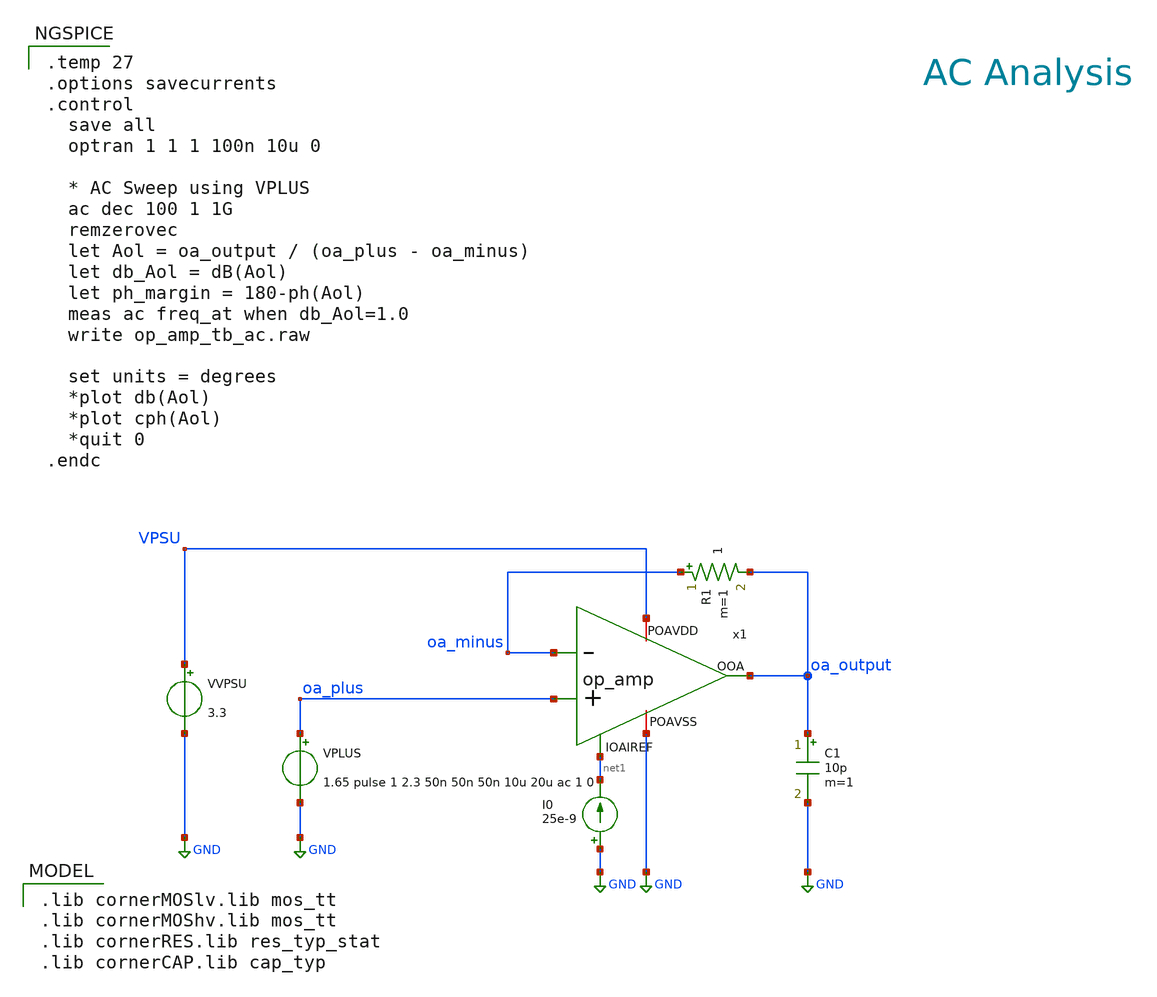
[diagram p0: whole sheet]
** sch_path: xschem/op_amp_tb_ac.sch
**.subckt op_amp_tb_ac
VVPSU VPSU GND 3.3
I0 GND net1 25e-9
x1 VPSU net1 oa_minus oa_output oa_plus GND op_amp
VPLUS oa_plus GND 1.65 pulse 1 2.3 50n 50n 50n 10u 20u ac 1 0
R1 oa_minus oa_output 1 m=1
C1 oa_output GND 10p m=1
**** begin user architecture code

.lib cornerMOSlv.lib mos_tt
.lib cornerMOShv.lib mos_tt
.lib cornerRES.lib res_typ_stat
.lib cornerCAP.lib cap_typ



.temp 27
.options savecurrents
.control
  save all
  optran 1 1 1 100n 10u 0

  * AC Sweep using VPLUS
  ac dec 100 1 1G
  remzerovec
  let Aol = oa_output / (oa_plus - oa_minus)
  let db_Aol = dB(Aol)
  let ph_margin = 180-ph(Aol)
  meas ac freq_at when db_Aol=1.0
  write op_amp_tb_ac.raw

  set units = degrees
  *plot db(Aol)
  *plot cph(Aol)
  *quit 0
.endc


**** end user architecture code
**.ends

* expanding   symbol:  op_amp.sym # of pins=6
** sym_path: xschem/op_amp.sym
** sch_path: xschem/op_amp.sch
.subckt op_amp POAVDD IOAIREF IOAM OOA IOAP POAVSS
*.iopin POAVDD
*.ipin IOAM
*.ipin IOAP
*.opin OOA
*.ipin IOAIREF
*.iopin POAVSS
XMP13 net1 net1 POAVDD POAVDD sg13_hv_pmos w=2.4u l=0.4u ng=1 m=1 mm_ok=1
XMP14 ptlg ptlg net1 POAVDD sg13_hv_pmos w=2.4u l=0.4u ng=1 m=1 mm_ok=1
XMN16 ptlg ncasc net2 POAVSS sg13_hv_nmos w=0.6u l=0.6u ng=1 m=1 mm_ok=1
XMN13 net2 nbias POAVSS POAVSS sg13_hv_nmos w=0.6u l=2.4u ng=1 m=1 mm_ok=1
XMN18 ntlg ntlg net3 POAVSS sg13_hv_nmos w=1.2u l=0.6u ng=1 m=1 mm_ok=1
XMN17 net3 net3 POAVSS POAVSS sg13_hv_nmos w=1.2u l=0.6u ng=1 m=1 mm_ok=1
XMP10 net13 pbias POAVDD POAVDD sg13_hv_pmos w=1.2u l=1.2u ng=1 m=1 mm_ok=1
XMP12 ntlg pcasc net13 POAVDD sg13_hv_pmos w=1.2u l=0.6u ng=1 m=1 mm_ok=1
XMP1 net9 pbias POAVDD POAVDD sg13_hv_pmos w=1.2u l=1.2u ng=1 m=4 mm_ok=1
XMP2 net10 pbias POAVDD POAVDD sg13_hv_pmos w=1.2u l=1.2u ng=1 m=4 mm_ok=1
XMN1 net9 IOAM net5 POAVSS sg13_hv_nmos w=4.8u l=0.45u ng=1 m=1 mm_ok=1
XMN2 net10 IOAP net5 POAVSS sg13_hv_nmos w=4.8u l=0.45u ng=1 m=1 mm_ok=1
XMN3 net4 nbias POAVSS POAVSS sg13_hv_nmos w=0.6u l=2.4u ng=1 m=8 mm_ok=1
XMN6 net5 ncasc net4 POAVSS sg13_hv_nmos w=0.6u l=0.6u ng=1 m=8 mm_ok=1
XMN7 net8 ncasc net7 POAVSS sg13_hv_nmos w=0.6u l=0.6u ng=1 m=8 mm_ok=1
XMN8 net12 ncasc net6 POAVSS sg13_hv_nmos w=0.6u l=0.6u ng=1 m=8 mm_ok=1
XMN4 net7 net8 POAVSS POAVSS sg13_hv_nmos w=0.6u l=2.4u ng=1 m=8 mm_ok=1
XMN5 net6 net8 POAVSS POAVSS sg13_hv_nmos w=0.6u l=2.4u ng=1 m=8 mm_ok=1
XMP3 net9 pbias POAVDD POAVDD sg13_hv_pmos w=1.2u l=1.2u ng=1 m=4 mm_ok=1
XMP5 net8 pcasc net9 POAVDD sg13_hv_pmos w=1.2u l=0.6u ng=1 m=8 mm_ok=1
XMP4 net10 pbias POAVDD POAVDD sg13_hv_pmos w=1.2u l=1.2u ng=1 m=4 mm_ok=1
XMP6 net11 pcasc net10 POAVDD sg13_hv_pmos w=1.2u l=0.6u ng=1 m=8 mm_ok=1
XMP7 net12 ptlg net11 POAVDD sg13_hv_pmos w=2.4u l=0.4u ng=1 m=4 mm_ok=1
XMN9 net11 ntlg net12 POAVSS sg13_hv_nmos w=1.2u l=0.6u ng=1 m=4 mm_ok=1
XMP8 OOA net11 POAVDD POAVDD sg13_hv_pmos w=2.4u l=0.4u ng=1 m=40 mm_ok=1
XMN10 OOA net12 POAVSS POAVSS sg13_hv_nmos w=1.2u l=0.6u ng=1 m=40 mm_ok=1
XC2 OOA net12 cap_cmim w=28.570e-6 l=14e-6 m=1 mm_ok=1
XC1 OOA net11 cap_cmim w=28.570e-6 l=14e-6 m=1 mm_ok=1
XMN20 IOAIREF IOAIREF POAVSS POAVSS sg13_hv_nmos w=0.6u l=2.4u ng=1 m=1 mm_ok=1
XMN21 pcasc IOAIREF POAVSS POAVSS sg13_hv_nmos w=0.6u l=2.4u ng=1 m=1 mm_ok=1
XMN22 pbias IOAIREF POAVSS POAVSS sg13_hv_nmos w=0.6u l=2.4u ng=1 m=1 mm_ok=1
XMN23 net21 ncasc POAVSS POAVSS sg13_hv_nmos w=0.4u l=10u ng=1 m=1 mm_ok=1
XMN25 net15 nbias POAVSS POAVSS sg13_hv_nmos w=0.6u l=2.4u ng=1 m=1 mm_ok=1
XMN24 ncasc ncasc net24 POAVSS sg13_hv_nmos w=0.4u l=10u ng=1 m=1 mm_ok=1
XMN26 nbias ncasc net15 POAVSS sg13_hv_nmos w=0.6u l=0.6u ng=1 m=1 mm_ok=1
XMP21 pcasc pcasc net20 POAVDD sg13_hv_pmos w=1u l=10u ng=1 m=1 mm_ok=1
XMP20 net20 pcasc net19 POAVDD sg13_hv_pmos w=1u l=10.0u ng=1 m=1 mm_ok=1
XMP22 net14 pbias POAVDD POAVDD sg13_hv_pmos w=1.2u l=1.2u ng=1 m=1 mm_ok=1
XMP25 pbias pcasc net14 POAVDD sg13_hv_pmos w=1.2u l=0.6u ng=1 m=1 mm_ok=1
XMP26 ncasc pcasc net17 POAVDD sg13_hv_pmos w=1.2u l=0.6u ng=1 m=1 mm_ok=1
XMP23 net17 pbias POAVDD POAVDD sg13_hv_pmos w=1.2u l=1.2u ng=1 m=1 mm_ok=1
XMP24 net16 pbias POAVDD POAVDD sg13_hv_pmos w=1.2u l=1.2u ng=1 m=1 mm_ok=1
XMP27 nbias pcasc net16 POAVDD sg13_hv_pmos w=1.2u l=0.6u ng=1 m=1 mm_ok=1
XMP16 net19 pcasc net18 POAVDD sg13_hv_pmos w=1u l=10.0u ng=1 m=1 mm_ok=1
XMN11 net22 ncasc net21 POAVSS sg13_hv_nmos w=0.4u l=10u ng=1 m=1 mm_ok=1
XMP28 net18 pcasc POAVDD POAVDD sg13_hv_pmos w=1u l=10.0u ng=1 m=1 mm_ok=1
XMN12 net23 ncasc net22 POAVSS sg13_hv_nmos w=0.4u l=10u ng=1 m=1 mm_ok=1
XMN14 net24 ncasc net23 POAVSS sg13_hv_nmos w=0.4u l=10u ng=1 m=1 mm_ok=1
XMDP1 POAVDD pbias POAVDD POAVDD sg13_hv_pmos w=1.2u l=1.2u ng=1 m=1 mm_ok=1
XMDP2 POAVDD pbias POAVDD POAVDD sg13_hv_pmos w=1.2u l=1.2u ng=1 m=1 mm_ok=1
XMDP3 POAVDD pcasc POAVDD POAVDD sg13_hv_pmos w=1.2u l=0.6u ng=1 m=1 mm_ok=1
XMDP4 POAVDD pcasc POAVDD POAVDD sg13_hv_pmos w=1.2u l=0.6u ng=1 m=1 mm_ok=1
XMDP5 POAVDD pcasc POAVDD POAVDD sg13_hv_pmos w=1.2u l=0.6u ng=1 m=1 mm_ok=1
XMDP6 POAVDD pcasc POAVDD POAVDD sg13_hv_pmos w=1.2u l=0.6u ng=1 m=1 mm_ok=1
XMDN1 POAVSS nbias POAVSS POAVSS sg13_hv_nmos w=0.6u l=2.4u ng=1 m=1 mm_ok=1
XMDN2 POAVSS nbias POAVSS POAVSS sg13_hv_nmos w=0.6u l=2.4u ng=1 m=1 mm_ok=1
XMDN3 POAVSS ncasc POAVSS POAVSS sg13_hv_nmos w=0.6u l=0.6u ng=1 m=1 mm_ok=1
XMDN4 POAVSS ncasc POAVSS POAVSS sg13_hv_nmos w=0.6u l=0.6u ng=1 m=1 mm_ok=1
XMDN5 POAVSS ncasc POAVSS POAVSS sg13_hv_nmos w=0.6u l=0.6u ng=1 m=1 mm_ok=1
XMDN6 POAVSS ncasc POAVSS POAVSS sg13_hv_nmos w=0.6u l=0.6u ng=1 m=1 mm_ok=1
XMDP7 POAVDD pbias POAVDD POAVDD sg13_hv_pmos w=1.2u l=1.2u ng=1 m=1 mm_ok=1
XMDP8 POAVDD pbias POAVDD POAVDD sg13_hv_pmos w=1.2u l=1.2u ng=1 m=1 mm_ok=1
XMDN7 POAVSS nbias POAVSS POAVSS sg13_hv_nmos w=0.6u l=2.4u ng=1 m=1 mm_ok=1
XMDN8 POAVSS nbias POAVSS POAVSS sg13_hv_nmos w=0.6u l=2.4u ng=1 m=1 mm_ok=1
XMDN9 POAVSS POAVSS POAVSS POAVSS sg13_hv_nmos w=1.2u l=0.45u ng=1 m=1 mm_ok=1
XMDN10 POAVSS POAVSS POAVSS POAVSS sg13_hv_nmos w=1.2u l=0.45u ng=1 m=1 mm_ok=1
XMDN11 POAVSS POAVSS POAVSS POAVSS sg13_hv_nmos w=1.2u l=0.45u ng=1 m=1 mm_ok=1
XMDN12 POAVSS POAVSS POAVSS POAVSS sg13_hv_nmos w=1.2u l=0.45u ng=1 m=1 mm_ok=1
XMDN13 POAVSS POAVSS POAVSS POAVSS sg13_hv_nmos w=2.4u l=0.45u ng=1 m=1 mm_ok=1
XMDN14 POAVSS POAVSS POAVSS POAVSS sg13_hv_nmos w=2.4u l=0.45u ng=1 m=1 mm_ok=1
XMDN15 POAVSS POAVSS POAVSS POAVSS sg13_hv_nmos w=2.4u l=0.45u ng=1 m=1 mm_ok=1
XMDN16 POAVSS POAVSS POAVSS POAVSS sg13_hv_nmos w=2.4u l=0.45u ng=1 m=1 mm_ok=1
XMDN17 POAVSS POAVSS POAVSS POAVSS sg13_hv_nmos w=1.2u l=0.45u ng=1 m=1 mm_ok=1
XMDN18 POAVSS POAVSS POAVSS POAVSS sg13_hv_nmos w=1.2u l=0.45u ng=1 m=1 mm_ok=1
XMDN19 POAVSS POAVSS POAVSS POAVSS sg13_hv_nmos w=1.2u l=0.45u ng=1 m=1 mm_ok=1
XMDN20 POAVSS POAVSS POAVSS POAVSS sg13_hv_nmos w=1.2u l=0.45u ng=1 m=1 mm_ok=1
XMDN21 POAVSS IOAIREF POAVSS POAVSS sg13_hv_nmos w=0.6u l=2.4u ng=1 m=1 mm_ok=1
XMDN22 POAVSS IOAIREF POAVSS POAVSS sg13_hv_nmos w=0.6u l=2.4u ng=1 m=1 mm_ok=1
XMDP9 POAVDD pcasc POAVDD POAVDD sg13_hv_pmos w=1u l=10u ng=1 m=1 mm_ok=1
XMDN23 POAVSS ncasc POAVSS POAVSS sg13_hv_nmos w=0.4u l=10u ng=1 m=1 mm_ok=1
XMDP10 POAVDD pcasc POAVDD POAVDD sg13_hv_pmos w=1u l=10u ng=1 m=1 mm_ok=1
XMDN24 POAVSS ncasc POAVSS POAVSS sg13_hv_nmos w=0.4u l=10u ng=1 m=1 mm_ok=1
XMDP11 POAVDD pbias POAVDD POAVDD sg13_hv_pmos w=1.2u l=1.2u ng=1 m=1 mm_ok=1
XMDP12 POAVDD pbias POAVDD POAVDD sg13_hv_pmos w=1.2u l=1.2u ng=1 m=1 mm_ok=1
XMDP13 POAVDD pcasc POAVDD POAVDD sg13_hv_pmos w=1.2u l=0.6u ng=1 m=1 mm_ok=1
XMDP14 POAVDD pcasc POAVDD POAVDD sg13_hv_pmos w=1.2u l=0.6u ng=1 m=1 mm_ok=1
XMDN25 POAVSS POAVSS POAVSS POAVSS sg13_hv_nmos w=0.6u l=2.4u ng=1 m=1 mm_ok=1
XMDN26 POAVSS POAVSS POAVSS POAVSS sg13_hv_nmos w=0.6u l=2.4u ng=1 m=1 mm_ok=1
XMDN27 POAVSS ncasc POAVSS POAVSS sg13_hv_nmos w=0.6u l=0.6u ng=1 m=1 mm_ok=1
XMDN28 POAVSS ncasc POAVSS POAVSS sg13_hv_nmos w=0.6u l=0.6u ng=1 m=1 mm_ok=1
XMDP15 POAVDD POAVDD POAVDD POAVDD sg13_hv_pmos w=2.4u l=0.4u ng=1 m=8 mm_ok=1
XMDN29 POAVSS POAVSS POAVSS POAVSS sg13_hv_nmos w=1.2u l=0.6u ng=1 m=8 mm_ok=1
XMDP16 POAVDD POAVDD POAVDD POAVDD sg13_hv_pmos w=2.4u l=0.4u ng=1 m=2 mm_ok=1
XMDN30 POAVSS POAVSS POAVSS POAVSS sg13_hv_nmos w=1.2u l=0.6u ng=1 m=2 mm_ok=1
XMDP17 POAVDD POAVDD POAVDD POAVDD sg13_hv_pmos w=2.4u l=0.4u ng=1 m=8 mm_ok=1
XMDN31 POAVSS POAVSS POAVSS POAVSS sg13_hv_nmos w=1.2u l=0.6u ng=1 m=8 mm_ok=1
.ends

.GLOBAL GND
.end
